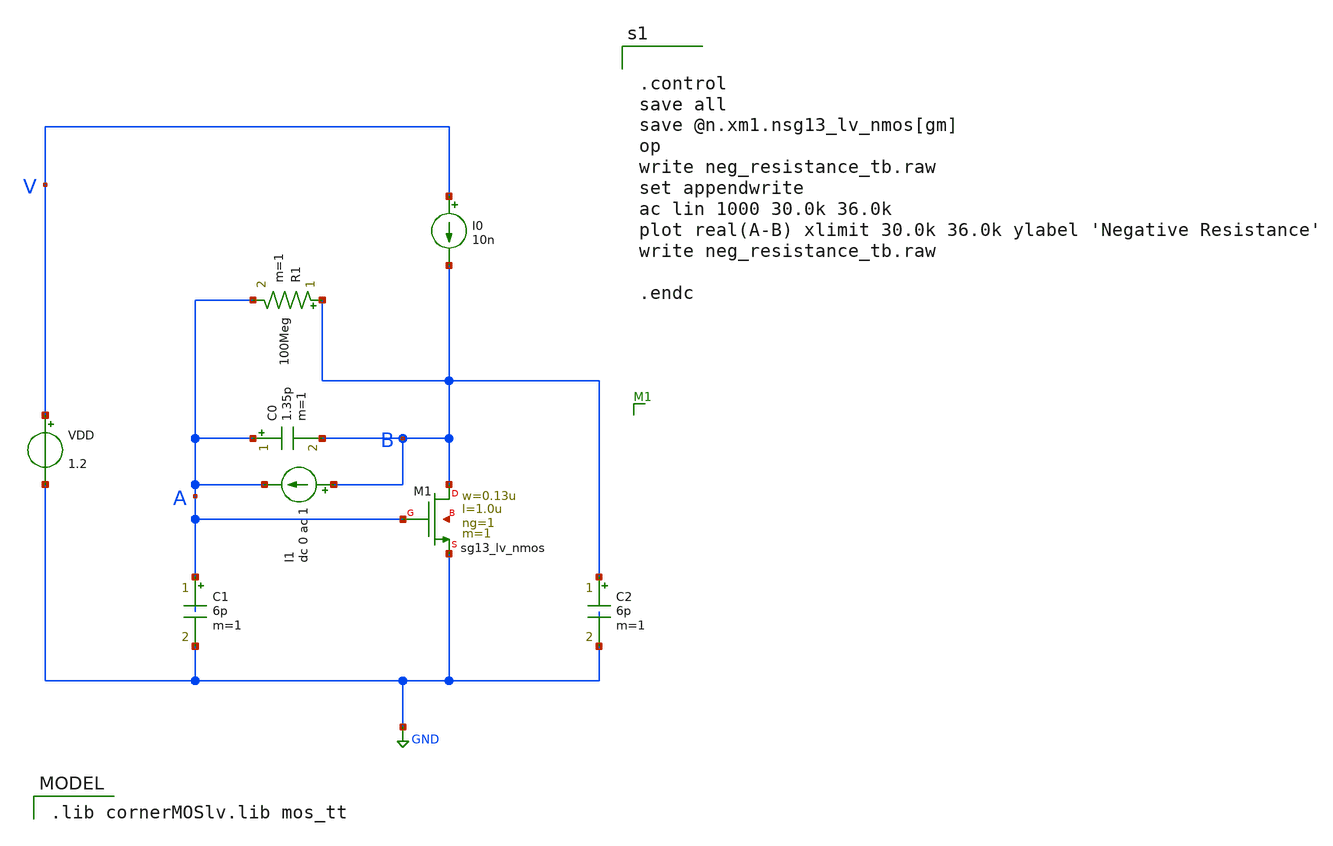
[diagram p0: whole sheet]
** sch_path: neg_resistance_tb.sch
**.subckt neg_resistance_tb
XM1 B A GND net1 sg13_lv_nmos w=0.13u l=1.0u ng=1 m=1 mm_ok=1
C1 A GND 6p m=1
C2 B GND 6p m=1
C0 A B 1.35p m=1
R1 B A 100Meg m=1
I0 V B 10n
I1 B A dc 0 ac 1
VDD V GND 1.2
**** begin user architecture code


.control
save all
save @n.xm1.nsg13_lv_nmos[gm]
op
write neg_resistance_tb.raw
set appendwrite
ac lin 1000 30.0k 36.0k
plot real(A-B) xlimit 30.0k 36.0k ylabel 'Negative Resistance'
write neg_resistance_tb.raw

.endc


 .lib cornerMOSlv.lib mos_tt

**** end user architecture code
**.ends
.GLOBAL GND
.end
